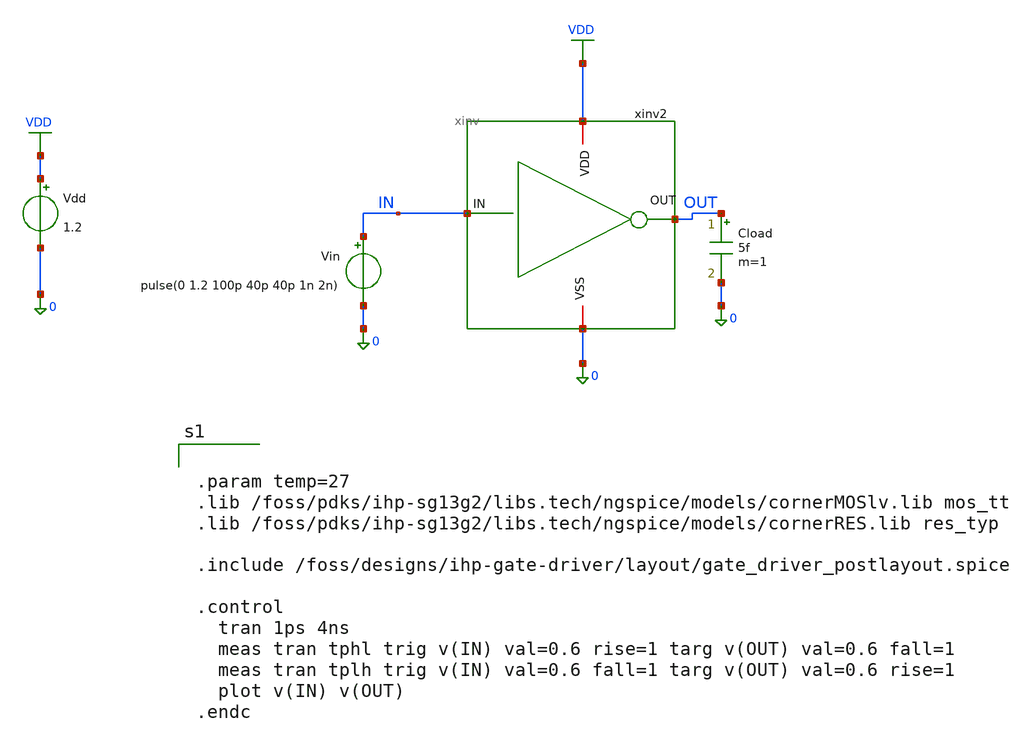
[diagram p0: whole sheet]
** sch_path: schematics/tb_gate_driver.sch
**.subckt tb_gate_driver
Vdd VDD 0 1.2
Vin IN 0 pulse(0 1.2 100p 40p 40p 1n 2n)
Cload OUT 0 5f m=1
xinv2 VDD OUT IN 0 xinv_pex
**** begin user architecture code


.param temp=27
.lib /foss/pdks/ihp-sg13g2/libs.tech/ngspice/models/cornerMOSlv.lib mos_tt
.lib /foss/pdks/ihp-sg13g2/libs.tech/ngspice/models/cornerRES.lib res_typ

.include /foss/designs/ihp-gate-driver/layout/gate_driver_postlayout.spice

.control
  tran 1ps 4ns
  meas tran tphl trig v(IN) val=0.6 rise=1 targ v(OUT) val=0.6 fall=1
  meas tran tplh trig v(IN) val=0.6 fall=1 targ v(OUT) val=0.6 rise=1
  plot v(IN) v(OUT)
.endc




**** end user architecture code
**.ends

* expanding   symbol:  /foss/designs/ihp-gate-driver/xinv.sym # of pins=4
** sym_path: schematics/xinv.sym
** sch_path: schematics/xinv.sch
.subckt xinv VDD OUT IN VSS
*.iopin VSS
*.iopin VDD
*.opin OUT
*.ipin IN
XM1 OUT IN VSS net2 sg13_lv_nmos w=5u l=0.13u ng=1 m=1 mm_ok=1
XM2 OUT IN VDD net1 sg13_lv_pmos w=10u l=0.13u ng=1 m=1 mm_ok=1
XR1 VSS net2 ptap1 R=262.8 w=0.78e-6 l=0.78e-6
XR2 VDD net1 ntap1 R=262.8 w=0.78e-6 l=0.78e-6
.ends

.GLOBAL VDD
.end
